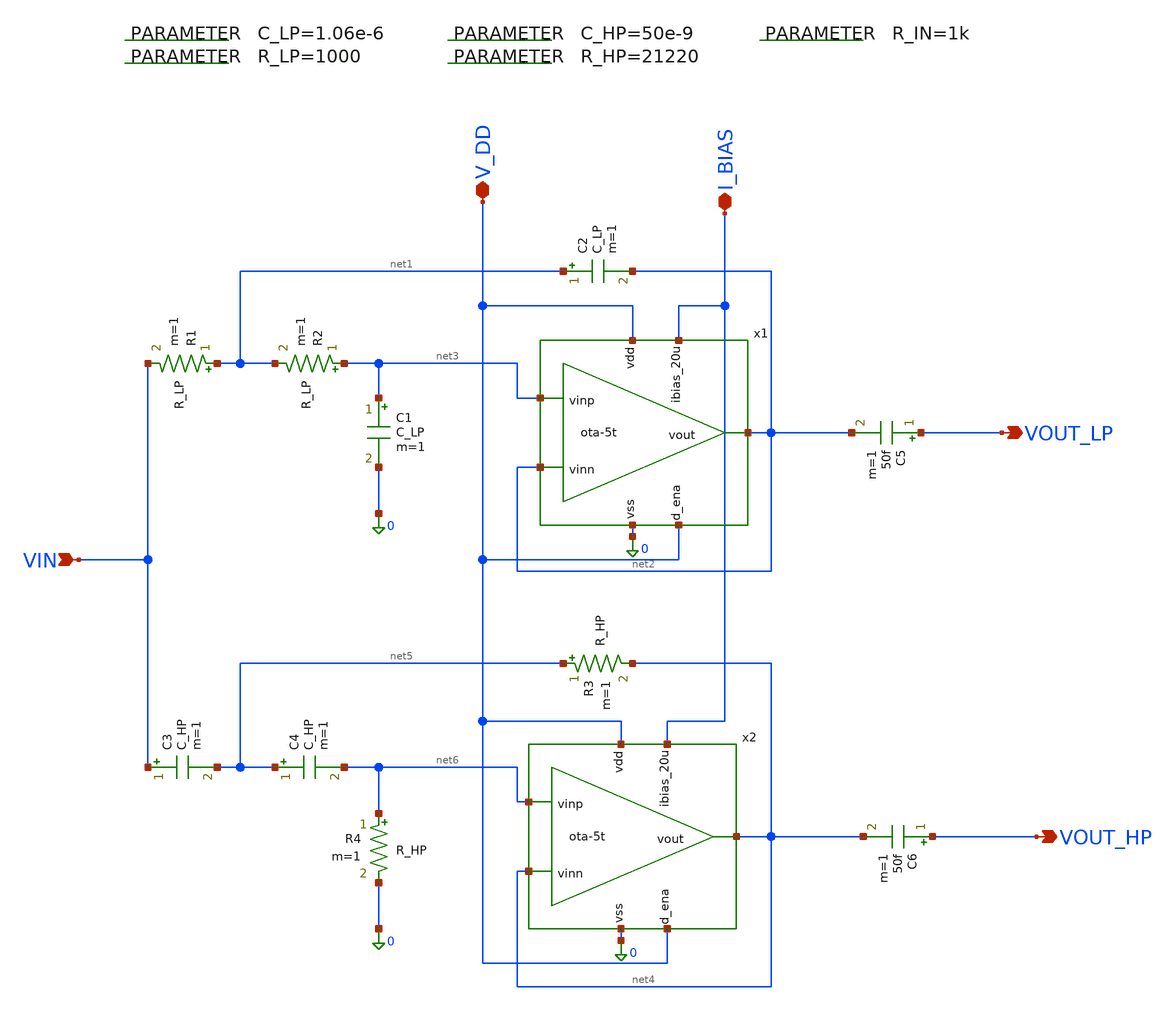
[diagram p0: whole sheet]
** sch_path: 004_Real_Circuits/linkwtz_riley_crossover_pretl_OTA_no_cross.sch
* 004_Real_Circuits/ota-5t.sch:
* (c) 2024-2025 Harald Pretl, Apache-2.0 license
**.subckt linkwtz_riley_crossover_pretl_OTA_no_cross VOUT_LP VOUT_HP VIN I_BIAS V_DD
*.opin VOUT_LP
*.opin VOUT_HP
*.ipin VIN
*.iopin I_BIAS
*.iopin V_DD
R1 net1 VIN R_LP m=1
.param C_LP=1.06e-6
.param R_LP=1000
.param C_HP=50e-9
.param R_HP=21220
.param R_IN=1k
R2 net3 net1 R_LP m=1
C1 net3 0 C_LP m=1
C2 net1 net2 C_LP m=1
C3 VIN net5 C_HP m=1
C4 net5 net6 C_HP m=1
R3 net5 net4 R_HP m=1
R4 net6 0 R_HP m=1
C5 VOUT_LP net2 50f m=1
C6 VOUT_HP net4 50f m=1
x1 V_DD net2 net3 net2 I_BIAS V_DD 0 ota-5t
x2 V_DD net4 net6 net4 I_BIAS V_DD 0 ota-5t
**.ends

* expanding   symbol:  /foss/designs/GitHub_Repo/004_Real_Circuits/ota-5t.sym # of pins=7
** sym_path: /foss/designs/GitHub_Repo/004_Real_Circuits/ota-5t.sym
** sch_path: /foss/designs/GitHub_Repo/004_Real_Circuits/ota-5t.sch
.subckt ota-5t vdd vout vinp vinn ibias_20u d_ena vss
*.ipin ibias_20u
*.iopin vdd
*.iopin vss
*.ipin vinp
*.ipin vinn
*.opin vout
*.ipin d_ena
XM5 tail gate_n vss vss sg13_lv_nmos w=1.0u l=5u ng=1 m=1 mm_ok=1
XM4 vout gate_p vdd vdd sg13_lv_pmos w=2.5u l=5u ng=1 m=1 mm_ok=1
XM1 gate_p vinp tail vss sg13_lv_nmos w=2u l=5u ng=1 m=1 mm_ok=1
XM2 vout vinn tail vss sg13_lv_nmos w=2u l=5u ng=1 m=1 mm_ok=1
XM3 gate_p gate_p vdd vdd sg13_lv_pmos w=2.5u l=5u ng=1 m=1 mm_ok=1
XM6 ibias_20u gate_n vss vss sg13_lv_nmos w=6.5u l=5u ng=5 m=1 mm_ok=1
XM9 gate_n ena_n vss vss sg13_lv_nmos w=0.5u l=0.13u ng=1 m=1 mm_ok=1
XM11 gate_p ena vdd vdd sg13_lv_pmos w=1.5u l=0.13u ng=1 m=1 mm_ok=1
XM7 ena ena_n vss vss sg13_lv_nmos w=0.5u l=0.13u ng=1 m=1 mm_ok=1
XM8 ena ena_n vdd vdd sg13_lv_pmos w=1.5u l=0.13u ng=1 m=1 mm_ok=1
XM10 ibias_20u ena gate_n vss sg13_lv_nmos w=0.5u l=0.13u ng=1 m=1 mm_ok=1
XM12 ena_n d_ena vss vss sg13_lv_nmos w=0.5u l=0.13u ng=1 m=1 mm_ok=1
XM13 ena_n d_ena vdd vdd sg13_lv_pmos w=1.5u l=0.13u ng=1 m=1 mm_ok=1
.ends

.end
